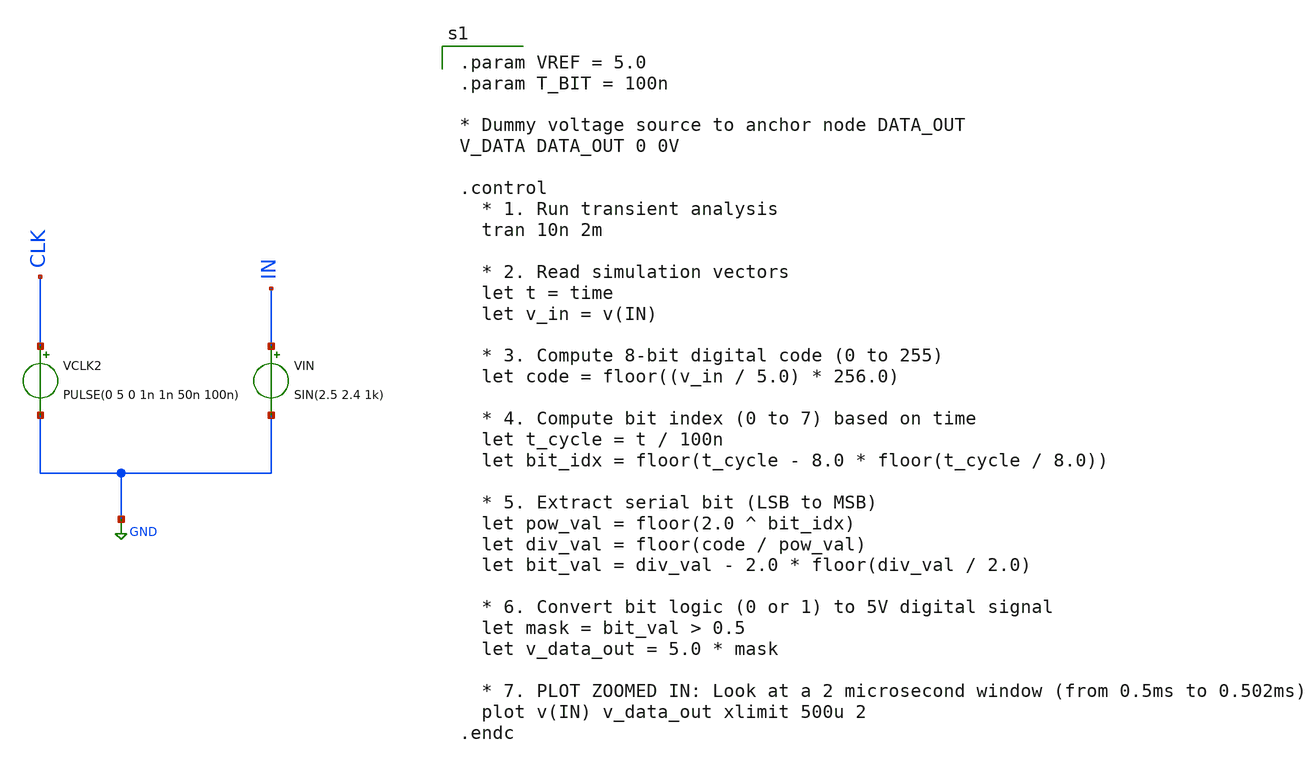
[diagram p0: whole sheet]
** sch_path: design/schematics/EIS/pkr_ideal_ADC.sch
**.subckt pkr_ideal_ADC
VIN IN GND SIN(2.5 2.4 1k)
VCLK2 CLK GND PULSE(0 5 0 1n 1n 50n 100n)
**** begin user architecture code

.param VREF = 5.0
.param T_BIT = 100n

* Dummy voltage source to anchor node DATA_OUT
V_DATA DATA_OUT 0 0V

.control
  * 1. Run transient analysis
  tran 10n 2m

  * 2. Read simulation vectors
  let t = time
  let v_in = v(IN)

  * 3. Compute 8-bit digital code (0 to 255)
  let code = floor((v_in / 5.0) * 256.0)

  * 4. Compute bit index (0 to 7) based on time
  let t_cycle = t / 100n
  let bit_idx = floor(t_cycle - 8.0 * floor(t_cycle / 8.0))

  * 5. Extract serial bit (LSB to MSB)
  let pow_val = floor(2.0 ^ bit_idx)
  let div_val = floor(code / pow_val)
  let bit_val = div_val - 2.0 * floor(div_val / 2.0)

  * 6. Convert bit logic (0 or 1) to 5V digital signal
  let mask = bit_val > 0.5
  let v_data_out = 5.0 * mask

  * 7. PLOT ZOOMED IN: Look at a 2 microsecond window (from 0.5ms to 0.502ms)
  plot v(IN) v_data_out xlimit 500u 2
.endc

**** end user architecture code
**.ends
.GLOBAL GND
.end
